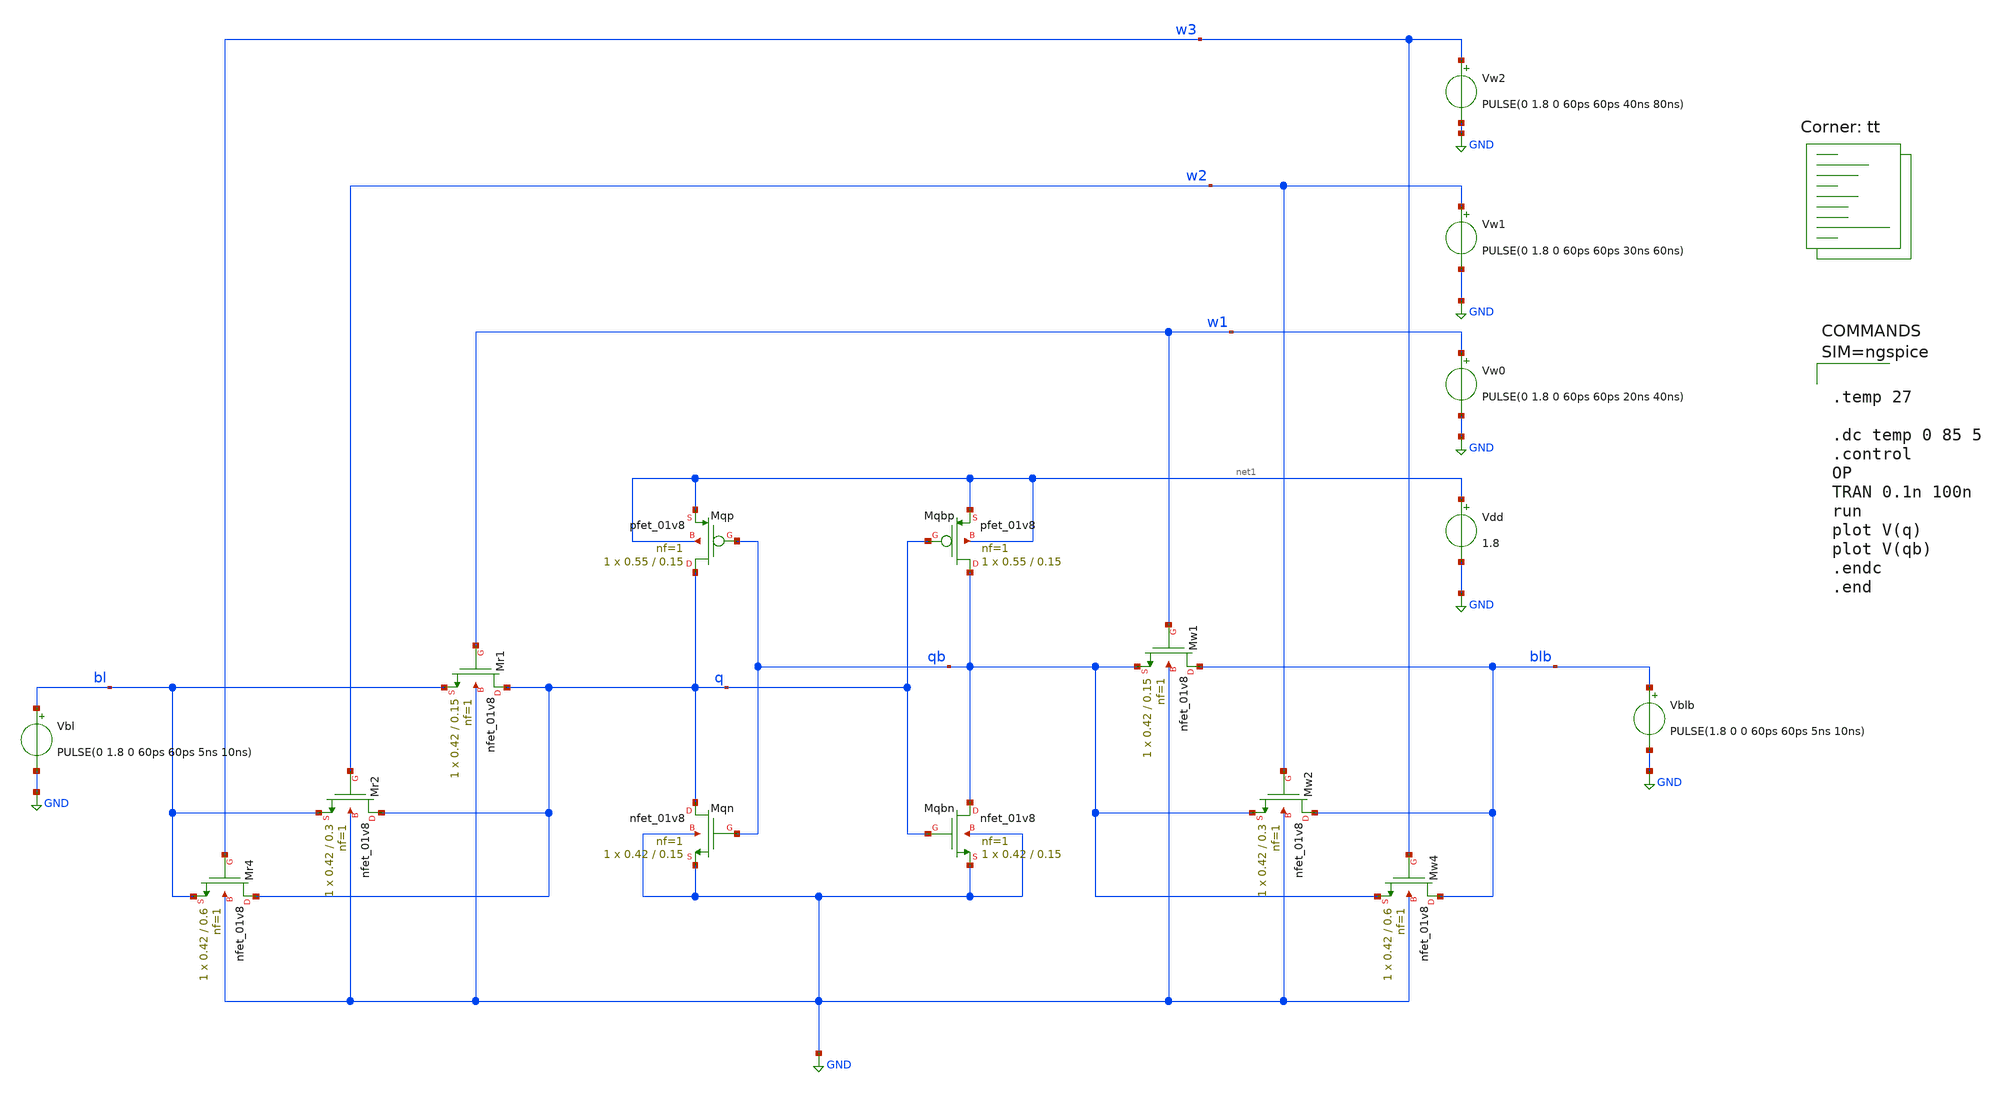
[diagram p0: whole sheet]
** sch_path: xschem/10T_SRAM.sch
**.subckt 10T_SRAM
XMqbn qb q GND GND sky130_fd_pr__nfet_01v8 L=0.15 W=0.42 nf=1 ad='int((1 + 1)/2) * 0.42 / 1 * 0.29' as='int((1 + 2)/2) * 0.42 / 1 * 0.29'
+ pd='2*int((1 + 1)/2) * (0.42 / 1 + 0.29)' ps='2*int((1 + 2)/2) * (0.42 / 1 + 0.29)' nrd='0.29 / 0.42 '
+ nrs='0.29 / 0.42 ' sa=0 sb=0 sd=0 mult=1 m=1
XMqn q qb GND GND sky130_fd_pr__nfet_01v8 L=0.15 W=0.42 nf=1 ad='int((1 + 1)/2) * 0.42 / 1 * 0.29' as='int((1 + 2)/2) * 0.42 / 1 * 0.29'
+ pd='2*int((1 + 1)/2) * (0.42 / 1 + 0.29)' ps='2*int((1 + 2)/2) * (0.42 / 1 + 0.29)' nrd='0.29 / 0.42 '
+ nrs='0.29 / 0.42 ' sa=0 sb=0 sd=0 mult=1 m=1
XMr1 q w1 bl GND sky130_fd_pr__nfet_01v8 L=0.15 W=0.42 nf=1 ad='int((1 + 1)/2) * 0.42 / 1 * 0.29' as='int((1 + 2)/2) * 0.42 / 1 * 0.29'
+ pd='2*int((1 + 1)/2) * (0.42 / 1 + 0.29)' ps='2*int((1 + 2)/2) * (0.42 / 1 + 0.29)' nrd='0.29 / 0.42 '
+ nrs='0.29 / 0.42 ' sa=0 sb=0 sd=0 mult=1 m=1
XMr2 q w2 bl GND sky130_fd_pr__nfet_01v8 L=0.3 W=0.42 nf=1 ad='int((1 + 1)/2) * 0.42 / 1 * 0.29' as='int((1 + 2)/2) * 0.42 / 1 * 0.29'
+ pd='2*int((1 + 1)/2) * (0.42 / 1 + 0.29)' ps='2*int((1 + 2)/2) * (0.42 / 1 + 0.29)' nrd='0.29 / 0.42 '
+ nrs='0.29 / 0.42 ' sa=0 sb=0 sd=0 mult=1 m=1
XMw1 blb w1 qb GND sky130_fd_pr__nfet_01v8 L=0.15 W=0.42 nf=1 ad='int((1 + 1)/2) * 0.42 / 1 * 0.29' as='int((1 + 2)/2) * 0.42 / 1 * 0.29'
+ pd='2*int((1 + 1)/2) * (0.42 / 1 + 0.29)' ps='2*int((1 + 2)/2) * (0.42 / 1 + 0.29)' nrd='0.29 / 0.42 '
+ nrs='0.29 / 0.42 ' sa=0 sb=0 sd=0 mult=1 m=1
XMw2 blb w2 qb GND sky130_fd_pr__nfet_01v8 L=0.3 W=0.42 nf=1 ad='int((1 + 1)/2) * 0.42 / 1 * 0.29' as='int((1 + 2)/2) * 0.42 / 1 * 0.29'
+ pd='2*int((1 + 1)/2) * (0.42 / 1 + 0.29)' ps='2*int((1 + 2)/2) * (0.42 / 1 + 0.29)' nrd='0.29 / 0.42 '
+ nrs='0.29 / 0.42 ' sa=0 sb=0 sd=0 mult=1 m=1
XMw4 blb w3 qb GND sky130_fd_pr__nfet_01v8 L=0.6 W=0.42 nf=1 ad='int((1 + 1)/2) * 0.42 / 1 * 0.29' as='int((1 + 2)/2) * 0.42 / 1 * 0.29'
+ pd='2*int((1 + 1)/2) * (0.42 / 1 + 0.29)' ps='2*int((1 + 2)/2) * (0.42 / 1 + 0.29)' nrd='0.29 / 0.42 '
+ nrs='0.29 / 0.42 ' sa=0 sb=0 sd=0 mult=1 m=1
XMr4 q w3 bl GND sky130_fd_pr__nfet_01v8 L=0.6 W=0.42 nf=1 ad='int((1 + 1)/2) * 0.42 / 1 * 0.29' as='int((1 + 2)/2) * 0.42 / 1 * 0.29'
+ pd='2*int((1 + 1)/2) * (0.42 / 1 + 0.29)' ps='2*int((1 + 2)/2) * (0.42 / 1 + 0.29)' nrd='0.29 / 0.42 '
+ nrs='0.29 / 0.42 ' sa=0 sb=0 sd=0 mult=1 m=1
XMqp q qb net1 net1 sky130_fd_pr__pfet_01v8 L=0.15 W=0.55 nf=1 ad='int((1 + 1)/2) * 0.55 / 1 * 0.29'
+ as='int((1 + 2)/2) * 0.55 / 1 * 0.29' pd='2*int((1 + 1)/2) * (0.55 / 1 + 0.29)' ps='2*int((1 + 2)/2) * (0.55 / 1 + 0.29)'
+ nrd='0.29 / 0.55 ' nrs='0.29 / 0.55 ' sa=0 sb=0 sd=0 mult=1 m=1
XMqbp qb q net1 net1 sky130_fd_pr__pfet_01v8 L=0.15 W=0.55 nf=1 ad='int((1 + 1)/2) * 0.55 / 1 * 0.29'
+ as='int((1 + 2)/2) * 0.55 / 1 * 0.29' pd='2*int((1 + 1)/2) * (0.55 / 1 + 0.29)' ps='2*int((1 + 2)/2) * (0.55 / 1 + 0.29)'
+ nrd='0.29 / 0.55 ' nrs='0.29 / 0.55 ' sa=0 sb=0 sd=0 mult=1 m=1
Vdd net1 GND 1.8
Vblb blb GND PULSE(1.8 0 0 60ps 60ps 5ns 10ns)
Vbl bl GND PULSE(0 1.8 0 60ps 60ps 5ns 10ns)
Vw0 w1 GND PULSE(0 1.8 0 60ps 60ps 20ns 40ns)
Vw1 w2 GND PULSE(0 1.8 0 60ps 60ps 30ns 60ns)
Vw2 w3 GND PULSE(0 1.8 0 60ps 60ps 40ns 80ns)
**** begin user architecture code
.lib $::SKYWATER_MODELS/sky130.lib.spice tt



.temp 27

.dc temp 0 85 5
.control
OP
TRAN 0.1n 100n
run
plot V(q)
plot V(qb)
.endc
.end



.lib /usr/local/share/pdk/sky130A/libs.tech/ngspice/sky130.lib.spice tt
**** end user architecture code
**.ends
.GLOBAL GND
.end
